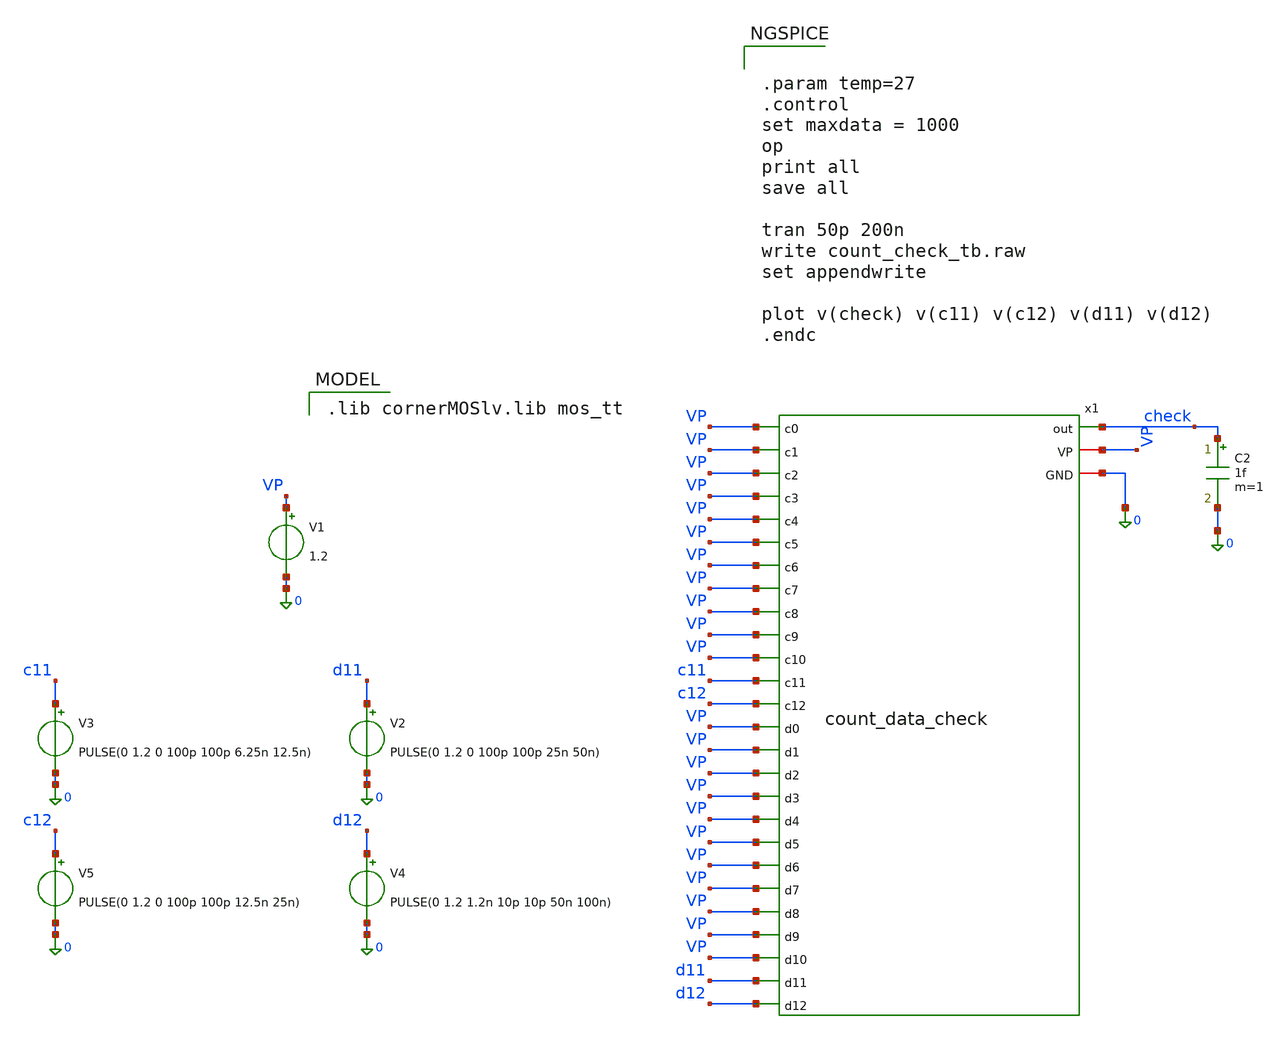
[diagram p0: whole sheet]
** sch_path: PLL0663-main/testbenches/tran/xschem/divider/count_check_tb.sch
**.subckt count_check_tb
V1 VP 0 1.2
C2 check 0 1f m=1
V3 c11 0 PULSE(0 1.2 0 100p 100p 6.25n 12.5n)
x1 check VP 0 VP VP VP VP VP VP VP VP VP VP VP c11 c12 VP VP VP VP VP VP VP VP VP VP VP d11 d12
+ count_data_check
V5 c12 0 PULSE(0 1.2 0 100p 100p 12.5n 25n)
V2 d11 0 PULSE(0 1.2 0 100p 100p 25n 50n)
V4 d12 0 PULSE(0 1.2 1.2n 10p 10p 50n 100n)
**** begin user architecture code
 .lib cornerMOSlv.lib mos_tt



.param temp=27
.control
set maxdata = 1000
op
print all
save all

tran 50p 200n
write count_check_tb.raw
set appendwrite

plot v(check) v(c11) v(c12) v(d11) v(d12)
.endc


**** end user architecture code
**.ends
.end
